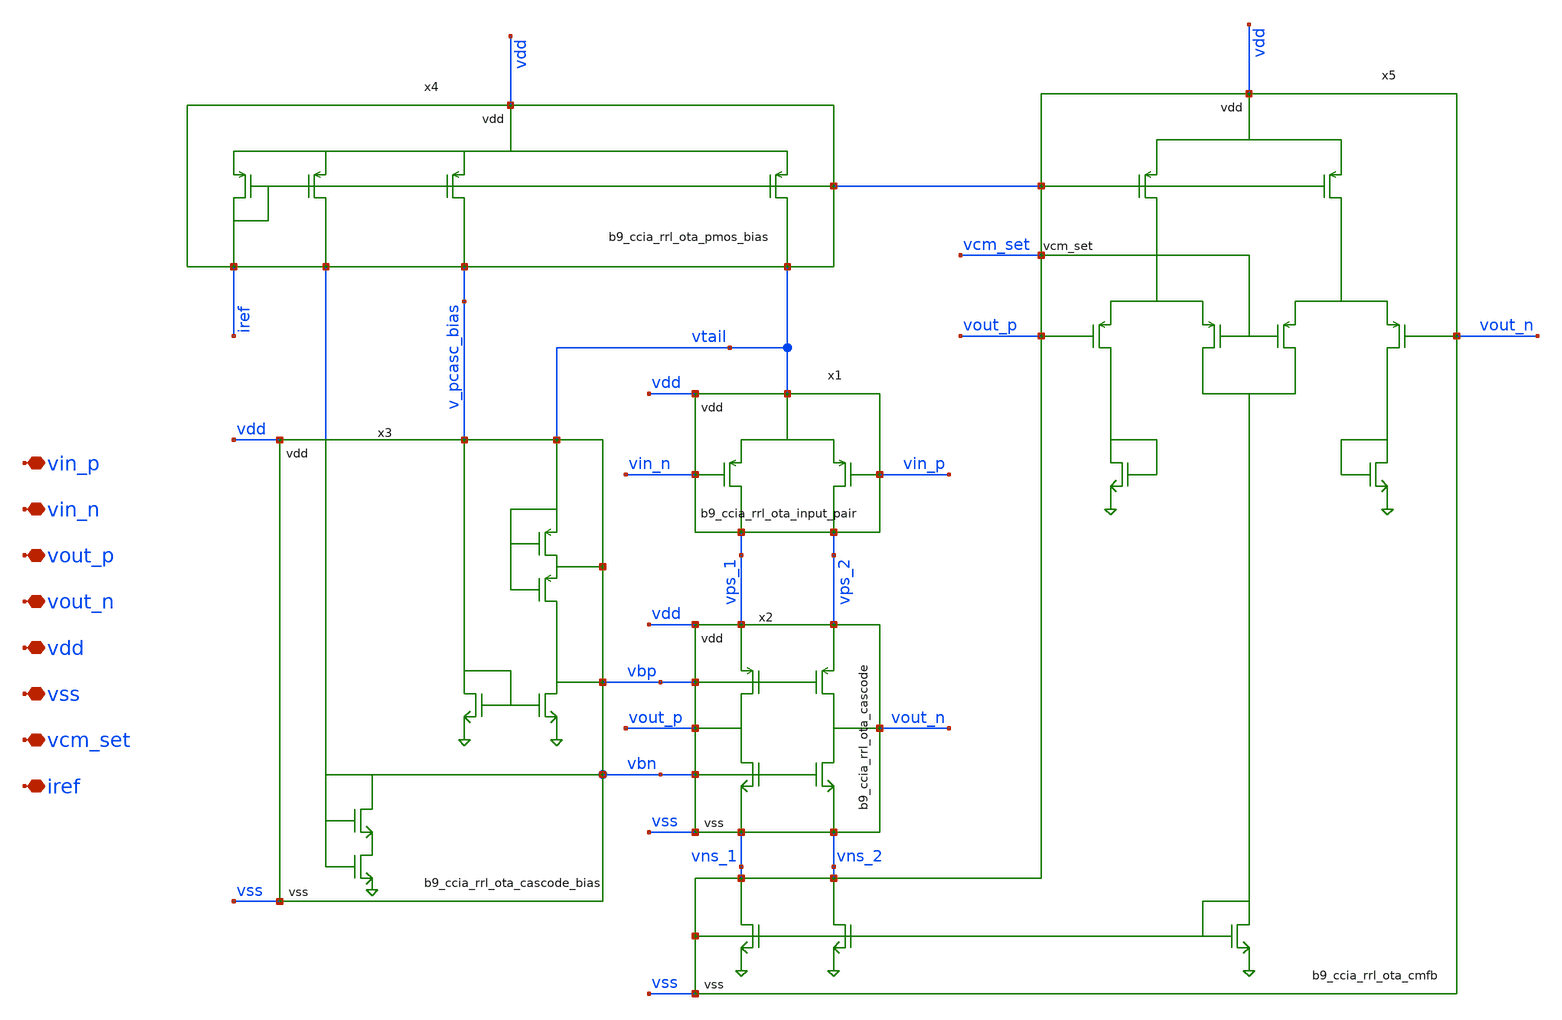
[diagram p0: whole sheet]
** sch_path: xschem/ccia_rrl_ota/b9_ccia_rrl_ota.sch
**.subckt b9_ccia_rrl_ota vin_p vin_n vout_p vout_n vdd vss vcm_set iref
*.iopin vin_p
*.iopin vin_n
*.iopin vout_p
*.iopin vout_n
*.iopin vdd
*.iopin vss
*.iopin vcm_set
*.iopin iref
x1 vtail vdd vin_n vin_p vps_1 vps_2 b9_ccia_rrl_ota_input_pair
x4 vdd vbn v_pcasc_bias vtail iref b9_ccia_rrl_ota_pmos_bias
x2 vdd vss vps_1 vps_2 vns_1 vns_2 vout_p vout_n vbp vbn b9_ccia_rrl_ota_cascode
x3 vbn v_pcasc_bias vtail vbp vss vdd net1 b9_ccia_rrl_ota_cascode_bias
x5 net2 vns_1 vns_2 vout_p vout_n iref vdd vss vcm_set b9_ccia_rrl_ota_cmfb
**.ends

* expanding   symbol:  xschem/ccia_rrl_ota/b9_ccia_rrl_ota_input_pair.sym # of pins=6
** sym_path: xschem/ccia_rrl_ota/b9_ccia_rrl_ota_input_pair.sym
** sch_path: xschem/ccia_rrl_ota/b9_ccia_rrl_ota_input_pair.sch
.subckt b9_ccia_rrl_ota_input_pair vtail vdd vin_1 vin_2 vd_1 vd_2
*.iopin vtail
*.iopin vdd
*.iopin vin_1
*.iopin vin_2
*.iopin vd_1
*.iopin vd_2
XM2 vd_1 vin_1 vtail vdd pfet_03v3 L=0.84u W=32u nf=8 ad='int((nf+1)/2) * W/nf * 0.18u' as='int((nf+2)/2) * W/nf * 0.18u'
+ pd='2*int((nf+1)/2) * (W/nf + 0.18u)' ps='2*int((nf+2)/2) * (W/nf + 0.18u)' nrd='0.18u / W' nrs='0.18u / W'
+ sa=0 sb=0 sd=0 m=1
XM3 vd_2 vin_2 vtail vdd pfet_03v3 L=0.84u W=32u nf=8 ad='int((nf+1)/2) * W/nf * 0.18u' as='int((nf+2)/2) * W/nf * 0.18u'
+ pd='2*int((nf+1)/2) * (W/nf + 0.18u)' ps='2*int((nf+2)/2) * (W/nf + 0.18u)' nrd='0.18u / W' nrs='0.18u / W'
+ sa=0 sb=0 sd=0 m=1
* noconn vtail
.ends


* expanding   symbol:  xschem/ccia_rrl_ota/b9_ccia_rrl_ota_pmos_bias.sym # of pins=6
** sym_path: xschem/ccia_rrl_ota/b9_ccia_rrl_ota_pmos_bias.sym
** sch_path: xschem/ccia_rrl_ota/b9_ccia_rrl_ota_pmos_bias.sch
.subckt b9_ccia_rrl_ota_pmos_bias vdd vbias_ncasc vbias_pcasc vtail iref
*.iopin vdd
*.iopin vbias_ncasc
*.iopin vbias_pcasc
*.iopin vtail
*.iopin iref
XM4 vtail iref vdd vdd pfet_03v3 L=3u W=4u nf=1 ad='int((nf+1)/2) * W/nf * 0.18u' as='int((nf+2)/2) * W/nf * 0.18u'
+ pd='2*int((nf+1)/2) * (W/nf + 0.18u)' ps='2*int((nf+2)/2) * (W/nf + 0.18u)' nrd='0.18u / W' nrs='0.18u / W'
+ sa=0 sb=0 sd=0 m=50
XM16 vbias_pcasc iref vdd vdd pfet_03v3 L=3u W=4u nf=1 ad='int((nf+1)/2) * W/nf * 0.18u' as='int((nf+2)/2) * W/nf * 0.18u'
+ pd='2*int((nf+1)/2) * (W/nf + 0.18u)' ps='2*int((nf+2)/2) * (W/nf + 0.18u)' nrd='0.18u / W' nrs='0.18u / W'
+ sa=0 sb=0 sd=0 m=10
XM17 vbias_ncasc iref vdd vdd pfet_03v3 L=3u W=4u nf=1 ad='int((nf+1)/2) * W/nf * 0.18u' as='int((nf+2)/2) * W/nf * 0.18u'
+ pd='2*int((nf+1)/2) * (W/nf + 0.18u)' ps='2*int((nf+2)/2) * (W/nf + 0.18u)' nrd='0.18u / W' nrs='0.18u / W'
+ sa=0 sb=0 sd=0 m=10
XM18 iref iref vdd vdd pfet_03v3 L=3u W=4u nf=1 ad='int((nf+1)/2) * W/nf * 0.18u' as='int((nf+2)/2) * W/nf * 0.18u'
+ pd='2*int((nf+1)/2) * (W/nf + 0.18u)' ps='2*int((nf+2)/2) * (W/nf + 0.18u)' nrd='0.18u / W' nrs='0.18u / W'
+ sa=0 sb=0 sd=0 m=10
.ends


* expanding   symbol:  xschem/ccia_rrl_ota/b9_ccia_rrl_ota_cascode.sym # of pins=10
** sym_path: xschem/ccia_rrl_ota/b9_ccia_rrl_ota_cascode.sym
** sch_path: xschem/ccia_rrl_ota/b9_ccia_rrl_ota_cascode.sch
.subckt b9_ccia_rrl_ota_cascode vdd vss pmos_vs_1 pmos_vs_2 nmos_vs_1 nmos_vs_2 vout_1 vout_2
+ pmos_vb nmos_vb
*.iopin vdd
*.iopin vss
*.iopin pmos_vs_1
*.iopin pmos_vs_2
*.iopin nmos_vs_1
*.iopin nmos_vs_2
*.iopin vout_1
*.iopin vout_2
*.iopin pmos_vb
*.iopin nmos_vb
XM10 vout_1 nmos_vb nmos_vs_1 vss nfet_03v3 L=0.28u W=6u nf=2 ad='int((nf+1)/2) * W/nf * 0.18u' as='int((nf+2)/2) * W/nf * 0.18u'
+ pd='2*int((nf+1)/2) * (W/nf + 0.18u)' ps='2*int((nf+2)/2) * (W/nf + 0.18u)' nrd='0.18u / W' nrs='0.18u / W'
+ sa=0 sb=0 sd=0 m=1
XM11 vout_2 nmos_vb nmos_vs_2 vss nfet_03v3 L=0.28u W=6u nf=2 ad='int((nf+1)/2) * W/nf * 0.18u' as='int((nf+2)/2) * W/nf * 0.18u'
+ pd='2*int((nf+1)/2) * (W/nf + 0.18u)' ps='2*int((nf+2)/2) * (W/nf + 0.18u)' nrd='0.18u / W' nrs='0.18u / W'
+ sa=0 sb=0 sd=0 m=1
XM7 vout_1 pmos_vb pmos_vs_1 vdd pfet_03v3 L=0.28u W=16u nf=4 ad='int((nf+1)/2) * W/nf * 0.18u' as='int((nf+2)/2) * W/nf * 0.18u'
+ pd='2*int((nf+1)/2) * (W/nf + 0.18u)' ps='2*int((nf+2)/2) * (W/nf + 0.18u)' nrd='0.18u / W' nrs='0.18u / W'
+ sa=0 sb=0 sd=0 m=1
XM8 vout_2 pmos_vb pmos_vs_2 vdd pfet_03v3 L=0.28u W=16u nf=4 ad='int((nf+1)/2) * W/nf * 0.18u' as='int((nf+2)/2) * W/nf * 0.18u'
+ pd='2*int((nf+1)/2) * (W/nf + 0.18u)' ps='2*int((nf+2)/2) * (W/nf + 0.18u)' nrd='0.18u / W' nrs='0.18u / W'
+ sa=0 sb=0 sd=0 m=1
.ends


* expanding   symbol:  xschem/ccia_rrl_ota/b9_ccia_rrl_ota_cascode_bias.sym # of pins=7
** sym_path: xschem/ccia_rrl_ota/b9_ccia_rrl_ota_cascode_bias.sym
** sch_path: xschem/ccia_rrl_ota/b9_ccia_rrl_ota_cascode_bias.sch
.subckt b9_ccia_rrl_ota_cascode_bias vb_nmos_casc bias vtail vb_pmos_casc vss vdd vdebug
*.iopin vb_nmos_casc
*.iopin bias
*.iopin vtail
*.iopin vb_pmos_casc
*.iopin vss
*.iopin vdd
*.iopin vdebug
XM1 net1 vb_nmos_casc vss vss nfet_03v3 L=3u W=2u nf=1 ad='int((nf+1)/2) * W/nf * 0.18u' as='int((nf+2)/2) * W/nf * 0.18u'
+ pd='2*int((nf+1)/2) * (W/nf + 0.18u)' ps='2*int((nf+2)/2) * (W/nf + 0.18u)' nrd='0.18u / W' nrs='0.18u / W'
+ sa=0 sb=0 sd=0 m=1
XM5 vdebug vb_pmos_casc vtail vdd pfet_03v3 L=0.84u W=8u nf=2 ad='int((nf+1)/2) * W/nf * 0.18u' as='int((nf+2)/2) * W/nf * 0.18u'
+ pd='2*int((nf+1)/2) * (W/nf + 0.18u)' ps='2*int((nf+2)/2) * (W/nf + 0.18u)' nrd='0.18u / W' nrs='0.18u / W'
+ sa=0 sb=0 sd=0 m=1
XM15 bias bias vss vss nfet_03v3 L=3u W=4.5u nf=1 ad='int((nf+1)/2) * W/nf * 0.18u' as='int((nf+2)/2) * W/nf * 0.18u'
+ pd='2*int((nf+1)/2) * (W/nf + 0.18u)' ps='2*int((nf+2)/2) * (W/nf + 0.18u)' nrd='0.18u / W' nrs='0.18u / W'
+ sa=0 sb=0 sd=0 m=1
XM9 vb_pmos_casc bias vss vss nfet_03v3 L=3u W=4.5u nf=1 ad='int((nf+1)/2) * W/nf * 0.18u' as='int((nf+2)/2) * W/nf * 0.18u'
+ pd='2*int((nf+1)/2) * (W/nf + 0.18u)' ps='2*int((nf+2)/2) * (W/nf + 0.18u)' nrd='0.18u / W' nrs='0.18u / W'
+ sa=0 sb=0 sd=0 m=1
XM6 vb_pmos_casc vb_pmos_casc vdebug vdd pfet_03v3 L=0.28u W=8u nf=2 ad='int((nf+1)/2) * W/nf * 0.18u'
+ as='int((nf+2)/2) * W/nf * 0.18u' pd='2*int((nf+1)/2) * (W/nf + 0.18u)' ps='2*int((nf+2)/2) * (W/nf + 0.18u)'
+ nrd='0.18u / W' nrs='0.18u / W' sa=0 sb=0 sd=0 m=1
XM14 vb_nmos_casc vb_nmos_casc net1 vss nfet_03v3 L=0.28u W=3u nf=1 ad='int((nf+1)/2) * W/nf * 0.18u'
+ as='int((nf+2)/2) * W/nf * 0.18u' pd='2*int((nf+1)/2) * (W/nf + 0.18u)' ps='2*int((nf+2)/2) * (W/nf + 0.18u)'
+ nrd='0.18u / W' nrs='0.18u / W' sa=0 sb=0 sd=0 m=1
.ends


* expanding   symbol:  xschem/ccia_rrl_ota/b9_ccia_rrl_ota_cmfb.sym # of pins=9
** sym_path: xschem/ccia_rrl_ota/b9_ccia_rrl_ota_cmfb.sym
** sch_path: xschem/ccia_rrl_ota/b9_ccia_rrl_ota_cmfb.sch
.subckt b9_ccia_rrl_ota_cmfb vb_nbias nmos_vs_1 nmos_vs_2 vout_1 vout_2 vg_pmos vdd vss vcm_set
*.iopin nmos_vs_1
*.iopin nmos_vs_2
*.iopin vout_1
*.iopin vout_2
*.iopin vg_pmos
*.iopin vdd
*.iopin vss
*.iopin vcm_set
*.iopin vb_nbias
XM12 nmos_vs_1 vb_nbias vss vss nfet_03v3 L=3u W=18u nf=4 ad='int((nf+1)/2) * W/nf * 0.18u' as='int((nf+2)/2) * W/nf * 0.18u'
+ pd='2*int((nf+1)/2) * (W/nf + 0.18u)' ps='2*int((nf+2)/2) * (W/nf + 0.18u)' nrd='0.18u / W' nrs='0.18u / W'
+ sa=0 sb=0 sd=0 m=1
XM13 nmos_vs_2 vb_nbias vss vss nfet_03v3 L=3u W=18u nf=4 ad='int((nf+1)/2) * W/nf * 0.18u' as='int((nf+2)/2) * W/nf * 0.18u'
+ pd='2*int((nf+1)/2) * (W/nf + 0.18u)' ps='2*int((nf+2)/2) * (W/nf + 0.18u)' nrd='0.18u / W' nrs='0.18u / W'
+ sa=0 sb=0 sd=0 m=1
XM19 vtail_cmfb1 vg_pmos vdd vdd pfet_03v3 L=3u W=4u nf=1 ad='int((nf+1)/2) * W/nf * 0.18u' as='int((nf+2)/2) * W/nf * 0.18u'
+ pd='2*int((nf+1)/2) * (W/nf + 0.18u)' ps='2*int((nf+2)/2) * (W/nf + 0.18u)' nrd='0.18u / W' nrs='0.18u / W'
+ sa=0 sb=0 sd=0 m=20
XM22 vtail_cmfb2 vg_pmos vdd vdd pfet_03v3 L=3u W=4u nf=1 ad='int((nf+1)/2) * W/nf * 0.18u' as='int((nf+2)/2) * W/nf * 0.18u'
+ pd='2*int((nf+1)/2) * (W/nf + 0.18u)' ps='2*int((nf+2)/2) * (W/nf + 0.18u)' nrd='0.18u / W' nrs='0.18u / W'
+ sa=0 sb=0 sd=0 m=20
XM25 vb_nbias vb_nbias vss vss nfet_03v3 L=3u W=18u nf=4 ad='int((nf+1)/2) * W/nf * 0.18u' as='int((nf+2)/2) * W/nf * 0.18u'
+ pd='2*int((nf+1)/2) * (W/nf + 0.18u)' ps='2*int((nf+2)/2) * (W/nf + 0.18u)' nrd='0.18u / W' nrs='0.18u / W'
+ sa=0 sb=0 sd=0 m=1
XM26 vcmfb_1 vcmfb_1 vss vss nfet_03v3 L=3u W=18u nf=2 ad='int((nf+1)/2) * W/nf * 0.18u' as='int((nf+2)/2) * W/nf * 0.18u'
+ pd='2*int((nf+1)/2) * (W/nf + 0.18u)' ps='2*int((nf+2)/2) * (W/nf + 0.18u)' nrd='0.18u / W' nrs='0.18u / W'
+ sa=0 sb=0 sd=0 m=1
XM27 vcmfb_2 vcmfb_2 vss vss nfet_03v3 L=3u W=18u nf=2 ad='int((nf+1)/2) * W/nf * 0.18u' as='int((nf+2)/2) * W/nf * 0.18u'
+ pd='2*int((nf+1)/2) * (W/nf + 0.18u)' ps='2*int((nf+2)/2) * (W/nf + 0.18u)' nrd='0.18u / W' nrs='0.18u / W'
+ sa=0 sb=0 sd=0 m=1
XM28 vcmfb_1 vout_1 vtail_cmfb1 vdd pfet_03v3 L=0.84u W=8u nf=2 ad='int((nf+1)/2) * W/nf * 0.18u' as='int((nf+2)/2) * W/nf * 0.18u'
+ pd='2*int((nf+1)/2) * (W/nf + 0.18u)' ps='2*int((nf+2)/2) * (W/nf + 0.18u)' nrd='0.18u / W' nrs='0.18u / W'
+ sa=0 sb=0 sd=0 m=1
XM20 vb_nbias vcm_set vtail_cmfb1 vdd pfet_03v3 L=0.84u W=8u nf=2 ad='int((nf+1)/2) * W/nf * 0.18u' as='int((nf+2)/2) * W/nf * 0.18u'
+ pd='2*int((nf+1)/2) * (W/nf + 0.18u)' ps='2*int((nf+2)/2) * (W/nf + 0.18u)' nrd='0.18u / W' nrs='0.18u / W'
+ sa=0 sb=0 sd=0 m=1
XM21 vb_nbias vcm_set vtail_cmfb2 vdd pfet_03v3 L=0.84u W=8u nf=2 ad='int((nf+1)/2) * W/nf * 0.18u' as='int((nf+2)/2) * W/nf * 0.18u'
+ pd='2*int((nf+1)/2) * (W/nf + 0.18u)' ps='2*int((nf+2)/2) * (W/nf + 0.18u)' nrd='0.18u / W' nrs='0.18u / W'
+ sa=0 sb=0 sd=0 m=1
XM23 vcmfb_2 vout_2 vtail_cmfb2 vdd pfet_03v3 L=0.84u W=8u nf=2 ad='int((nf+1)/2) * W/nf * 0.18u' as='int((nf+2)/2) * W/nf * 0.18u'
+ pd='2*int((nf+1)/2) * (W/nf + 0.18u)' ps='2*int((nf+2)/2) * (W/nf + 0.18u)' nrd='0.18u / W' nrs='0.18u / W'
+ sa=0 sb=0 sd=0 m=1
.ends

.end
